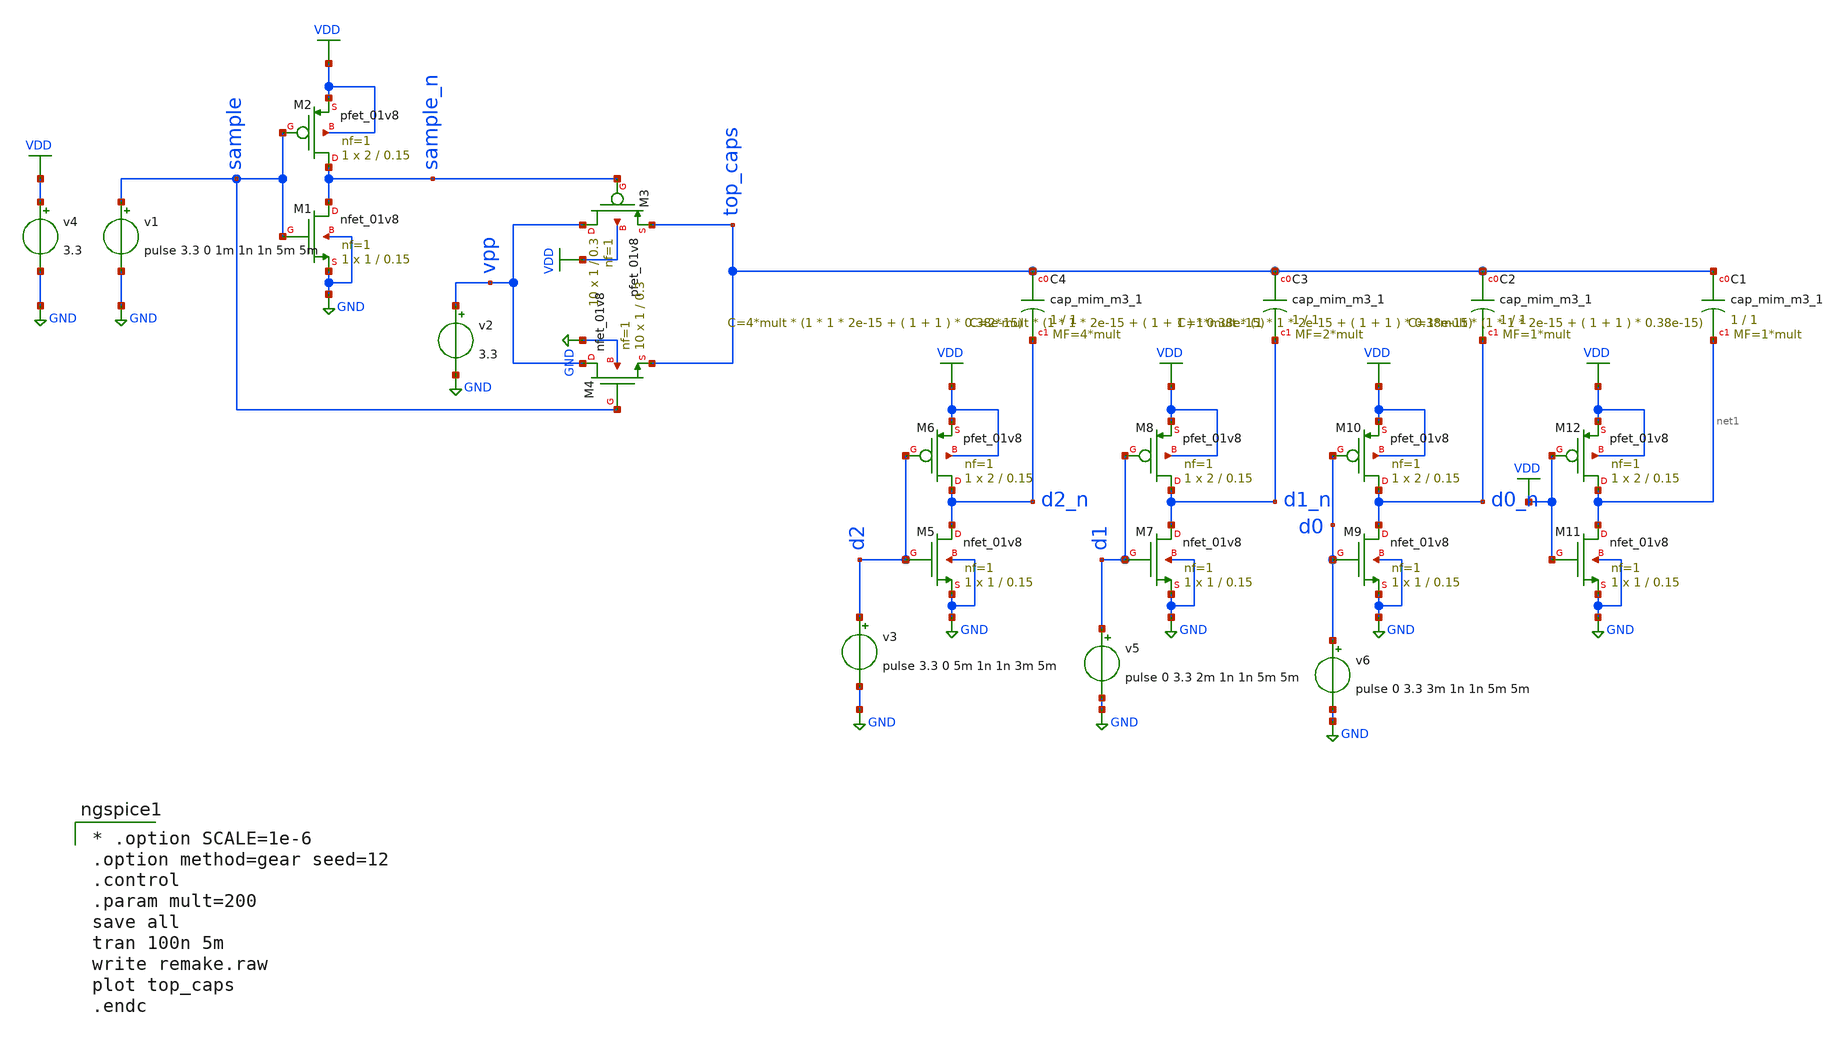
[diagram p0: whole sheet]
** sch_path: Schematics/ADC/simulations_elements/deprecated/remake.sch
**.subckt remake
v1 sample GND pulse 3.3 0 1m 1n 1n 5m 5m
v4 VDD GND 3.3
XM1 sample_n sample GND GND sky130_fd_pr__nfet_01v8 L=0.15 W=1 nf=1 ad='int((nf+1)/2) * W/nf * 0.29'
+ as='int((nf+2)/2) * W/nf * 0.29' pd='2*int((nf+1)/2) * (W/nf + 0.29)' ps='2*int((nf+2)/2) * (W/nf + 0.29)'
+ nrd='0.29 / W' nrs='0.29 / W' sa=0 sb=0 sd=0 mult=1 m=1
XM2 sample_n sample VDD VDD sky130_fd_pr__pfet_01v8 L=0.15 W=2 nf=1 ad='int((nf+1)/2) * W/nf * 0.29'
+ as='int((nf+2)/2) * W/nf * 0.29' pd='2*int((nf+1)/2) * (W/nf + 0.29)' ps='2*int((nf+2)/2) * (W/nf + 0.29)'
+ nrd='0.29 / W' nrs='0.29 / W' sa=0 sb=0 sd=0 mult=1 m=1
XM3 vpp sample_n top_caps VDD sky130_fd_pr__pfet_01v8 L=0.3 W=1 nf=1 ad='int((nf+1)/2) * W/nf * 0.29'
+ as='int((nf+2)/2) * W/nf * 0.29' pd='2*int((nf+1)/2) * (W/nf + 0.29)' ps='2*int((nf+2)/2) * (W/nf + 0.29)'
+ nrd='0.29 / W' nrs='0.29 / W' sa=0 sb=0 sd=0 mult=10 m=10
XM4 vpp sample top_caps GND sky130_fd_pr__nfet_01v8 L=0.3 W=1 nf=1 ad='int((nf+1)/2) * W/nf * 0.29' as='int((nf+2)/2) * W/nf * 0.29'
+ pd='2*int((nf+1)/2) * (W/nf + 0.29)' ps='2*int((nf+2)/2) * (W/nf + 0.29)' nrd='0.29 / W' nrs='0.29 / W'
+ sa=0 sb=0 sd=0 mult=10 m=10
v2 vpp GND 3.3
XM5 d2_n d2 GND GND sky130_fd_pr__nfet_01v8 L=0.15 W=1 nf=1 ad='int((nf+1)/2) * W/nf * 0.29' as='int((nf+2)/2) * W/nf * 0.29'
+ pd='2*int((nf+1)/2) * (W/nf + 0.29)' ps='2*int((nf+2)/2) * (W/nf + 0.29)' nrd='0.29 / W' nrs='0.29 / W'
+ sa=0 sb=0 sd=0 mult=1 m=1
XM6 d2_n d2 VDD VDD sky130_fd_pr__pfet_01v8 L=0.15 W=2 nf=1 ad='int((nf+1)/2) * W/nf * 0.29' as='int((nf+2)/2) * W/nf * 0.29'
+ pd='2*int((nf+1)/2) * (W/nf + 0.29)' ps='2*int((nf+2)/2) * (W/nf + 0.29)' nrd='0.29 / W' nrs='0.29 / W'
+ sa=0 sb=0 sd=0 mult=1 m=1
XM7 d1_n d1 GND GND sky130_fd_pr__nfet_01v8 L=0.15 W=1 nf=1 ad='int((nf+1)/2) * W/nf * 0.29' as='int((nf+2)/2) * W/nf * 0.29'
+ pd='2*int((nf+1)/2) * (W/nf + 0.29)' ps='2*int((nf+2)/2) * (W/nf + 0.29)' nrd='0.29 / W' nrs='0.29 / W'
+ sa=0 sb=0 sd=0 mult=1 m=1
XM8 d1_n d1 VDD VDD sky130_fd_pr__pfet_01v8 L=0.15 W=2 nf=1 ad='int((nf+1)/2) * W/nf * 0.29' as='int((nf+2)/2) * W/nf * 0.29'
+ pd='2*int((nf+1)/2) * (W/nf + 0.29)' ps='2*int((nf+2)/2) * (W/nf + 0.29)' nrd='0.29 / W' nrs='0.29 / W'
+ sa=0 sb=0 sd=0 mult=1 m=1
XM9 d0_n d0 GND GND sky130_fd_pr__nfet_01v8 L=0.15 W=1 nf=1 ad='int((nf+1)/2) * W/nf * 0.29' as='int((nf+2)/2) * W/nf * 0.29'
+ pd='2*int((nf+1)/2) * (W/nf + 0.29)' ps='2*int((nf+2)/2) * (W/nf + 0.29)' nrd='0.29 / W' nrs='0.29 / W'
+ sa=0 sb=0 sd=0 mult=1 m=1
XM10 d0_n d0 VDD VDD sky130_fd_pr__pfet_01v8 L=0.15 W=2 nf=1 ad='int((nf+1)/2) * W/nf * 0.29' as='int((nf+2)/2) * W/nf * 0.29'
+ pd='2*int((nf+1)/2) * (W/nf + 0.29)' ps='2*int((nf+2)/2) * (W/nf + 0.29)' nrd='0.29 / W' nrs='0.29 / W'
+ sa=0 sb=0 sd=0 mult=1 m=1
XM11 net1 VDD GND GND sky130_fd_pr__nfet_01v8 L=0.15 W=1 nf=1 ad='int((nf+1)/2) * W/nf * 0.29' as='int((nf+2)/2) * W/nf * 0.29'
+ pd='2*int((nf+1)/2) * (W/nf + 0.29)' ps='2*int((nf+2)/2) * (W/nf + 0.29)' nrd='0.29 / W' nrs='0.29 / W'
+ sa=0 sb=0 sd=0 mult=1 m=1
XM12 net1 VDD VDD VDD sky130_fd_pr__pfet_01v8 L=0.15 W=2 nf=1 ad='int((nf+1)/2) * W/nf * 0.29' as='int((nf+2)/2) * W/nf * 0.29'
+ pd='2*int((nf+1)/2) * (W/nf + 0.29)' ps='2*int((nf+2)/2) * (W/nf + 0.29)' nrd='0.29 / W' nrs='0.29 / W'
+ sa=0 sb=0 sd=0 mult=1 m=1
XC1 top_caps net1 sky130_fd_pr__cap_mim_m3_1 W=1 L=1 MF=1*mult m=1*mult
XC2 top_caps d0_n sky130_fd_pr__cap_mim_m3_1 W=1 L=1 MF=1*mult m=1*mult
XC3 top_caps d1_n sky130_fd_pr__cap_mim_m3_1 W=1 L=1 MF=2*mult m=2*mult
XC4 top_caps d2_n sky130_fd_pr__cap_mim_m3_1 W=1 L=1 MF=4*mult m=4*mult
v3 d2 GND pulse 3.3 0 5m 1n 1n 3m 5m
v5 d1 GND pulse 0 3.3 2m 1n 1n 5m 5m
v6 d0 GND pulse 0 3.3 3m 1n 1n 5m 5m
**** begin user architecture code

** opencircuitdesign pdks install
.lib $::SKYWATER_MODELS/sky130.lib.spice tt


**** end user architecture code
**.ends
.GLOBAL GND
.GLOBAL VDD
**** begin user architecture code

* .option SCALE=1e-6
.option method=gear seed=12
.control
.param mult=200
save all
tran 100n 5m
write remake.raw
plot top_caps
.endc


**** end user architecture code
.end
